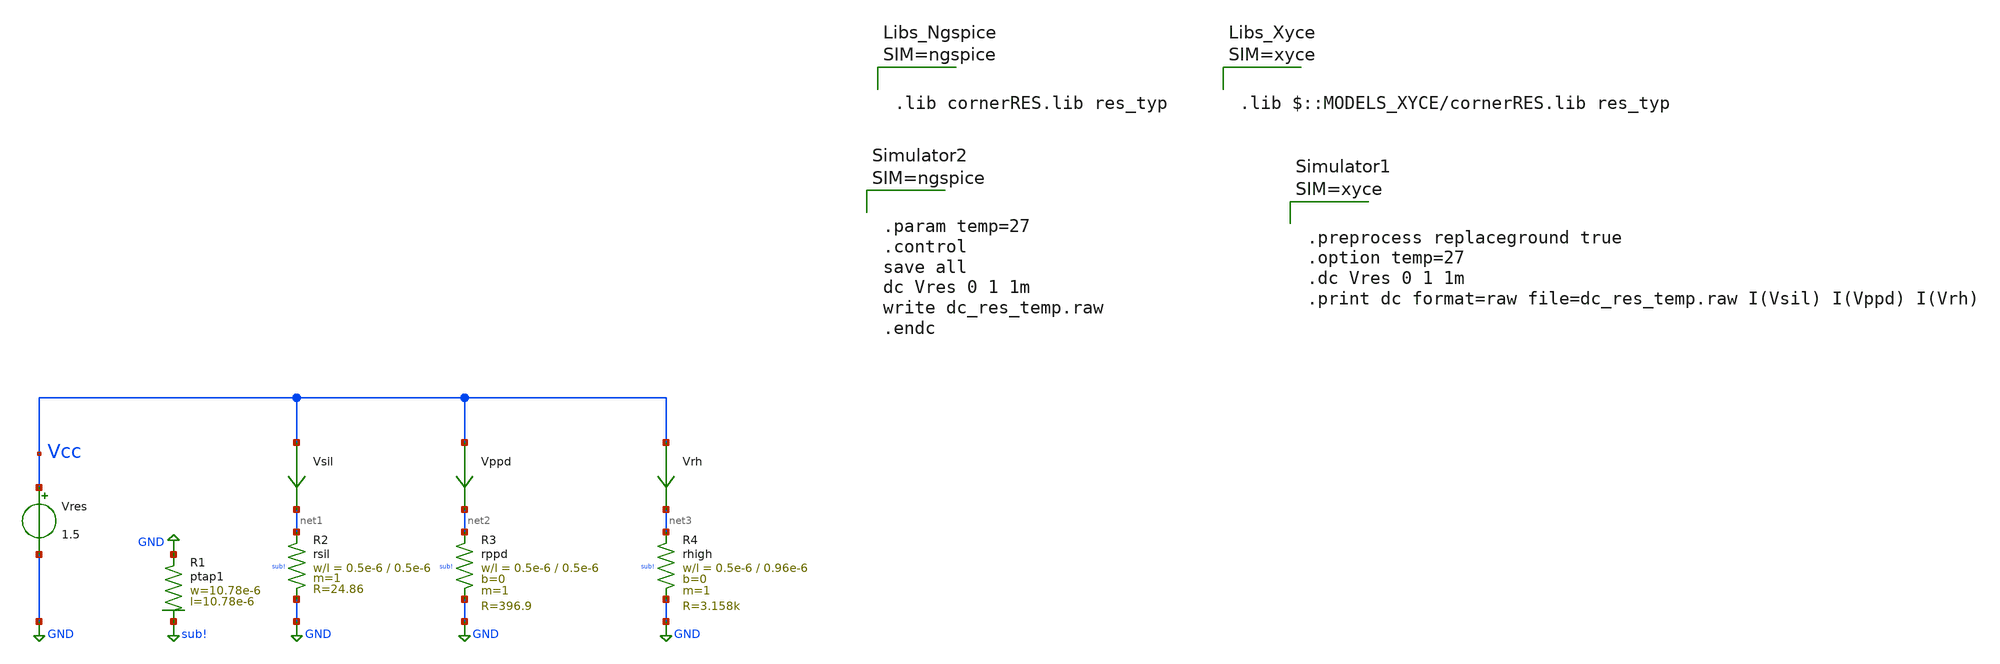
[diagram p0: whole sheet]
** sch_path: ihp-sg13g2/libs.tech/xschem/sg13g2_tests_xyce/dc_res_temp.sch
* Copyright 2023 IHP PDK Authors
**.subckt dc_res_temp
Vres Vcc GND 1.5
Vsil Vcc net1 0
.save i(vsil)
Vppd Vcc net2 0
.save i(vppd)
Vrh Vcc net3 0
.save i(vrh)
XR1 GND sub! ptap1 R=6.151 w=10.78e-6 l=10.78e-6
XR2 net1 GND sub! rsil w=0.5e-6 l=0.5e-6 m=1 mm_ok=1
XR3 net2 GND sub! rppd w=0.5e-6 l=0.5e-6 m=1 b=0 mm_ok=1
XR4 net3 GND sub! rhigh w=0.5e-6 l=0.96e-6 m=1 b=0 mm_ok=1
**** begin user architecture code









.lib cornerRES.lib res_typ






.param temp=27
.control
save all
dc Vres 0 1 1m
write dc_res_temp.raw
.endc



**** end user architecture code
**.ends
.GLOBAL GND
.GLOBAL sub!
.end
